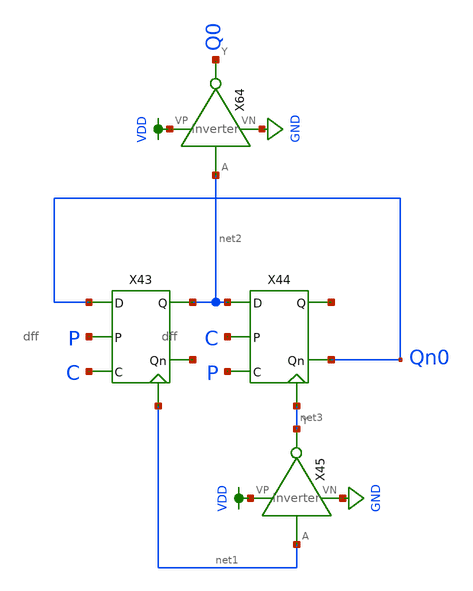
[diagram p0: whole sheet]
** sch_path: schematic/counter-b0_lvs.sch
**.subckt counter-b0_lvs
X43 Qn0 net4 net2 net1 P C dff
X44 net2 Qn0 net5 net3 C P dff
X45 net1 net3 VDD GND inverter
X64 net2 Q0 VDD GND inverter
**.ends
.GLOBAL VDD
.GLOBAL GND
.end
